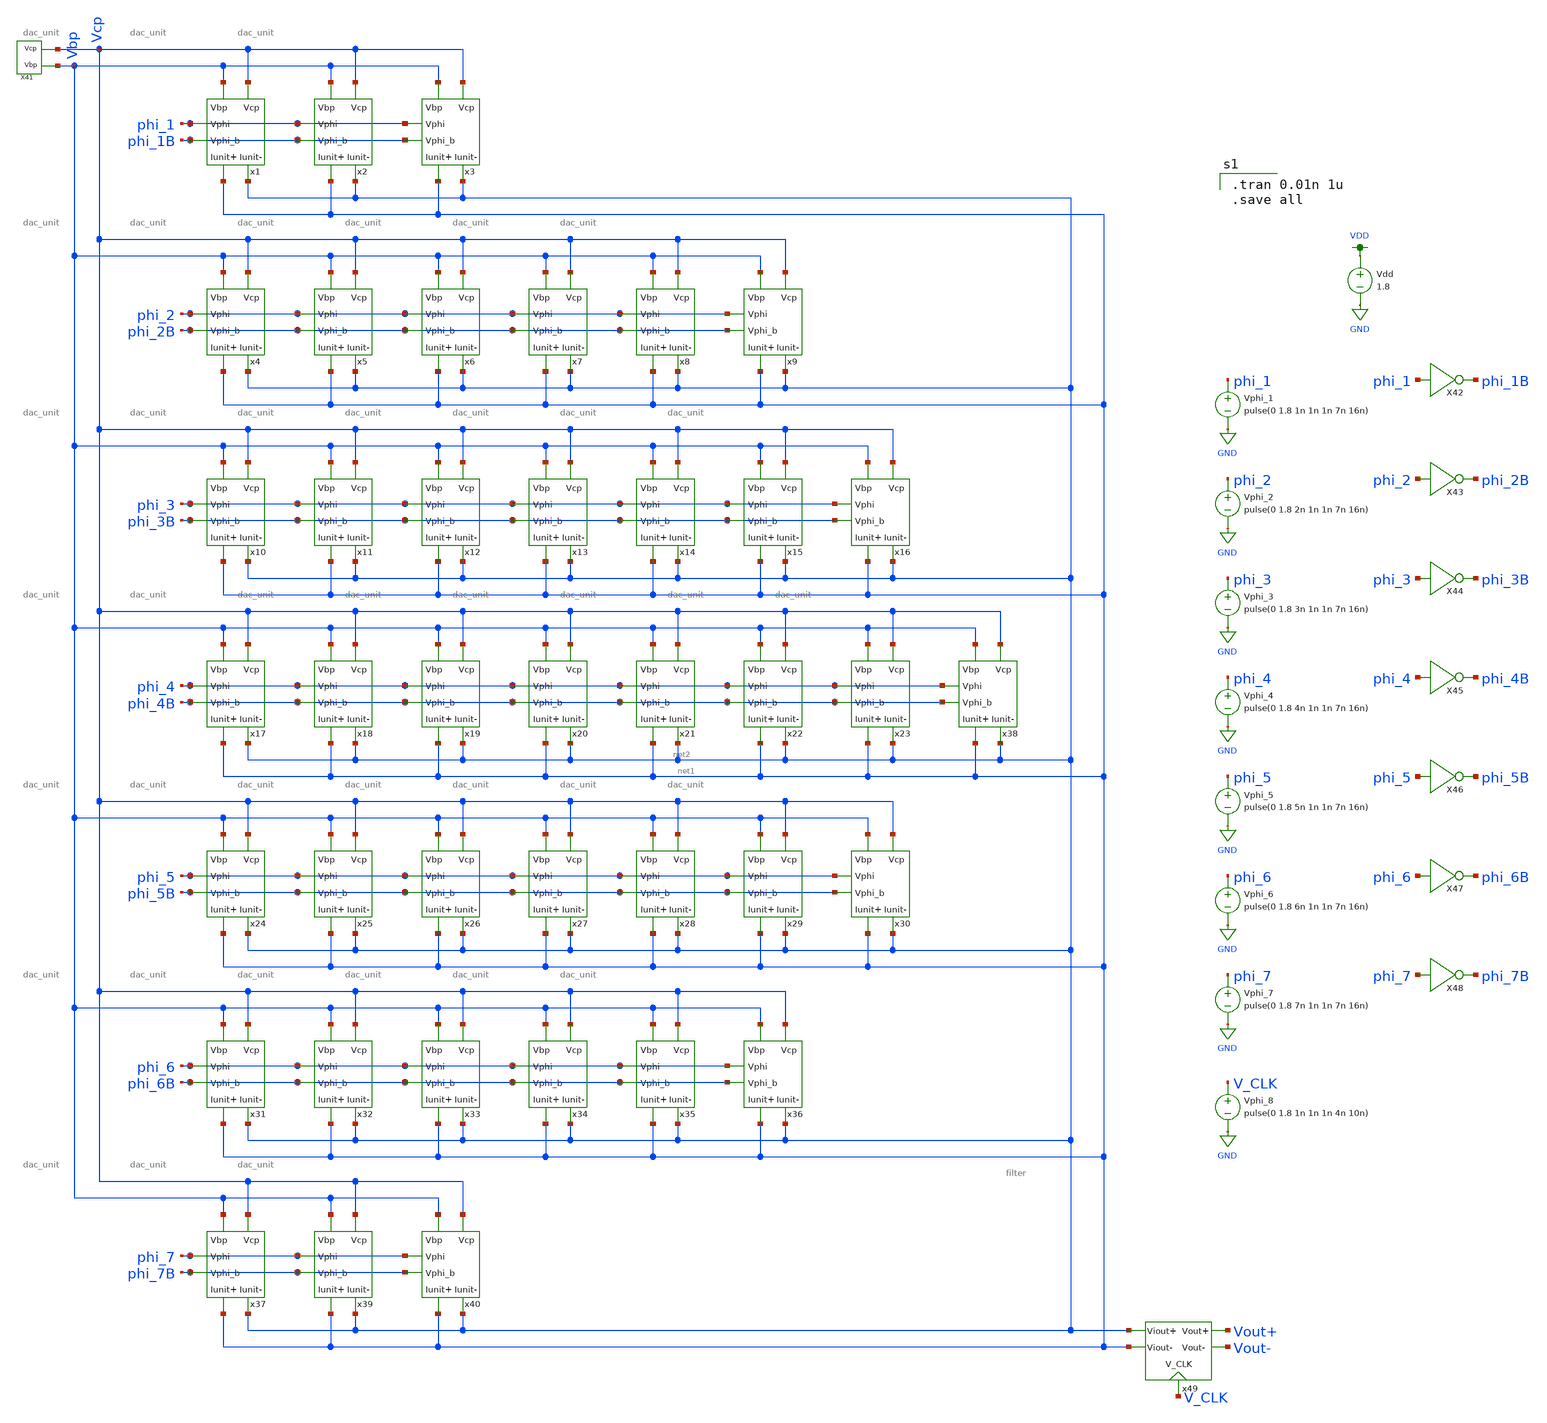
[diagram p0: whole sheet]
** sch_path: simulation/archived/dac_tran (copy).sch
**.subckt dac_tran (copy)
x1 Vbp Vcp net1 net2 phi_1 phi_1B dac_unit
x2 Vbp Vcp net1 net2 phi_1 phi_1B dac_unit
x3 Vbp Vcp net1 net2 phi_1 phi_1B dac_unit
x4 Vbp Vcp net1 net2 phi_2 phi_2B dac_unit
x5 Vbp Vcp net1 net2 phi_2 phi_2B dac_unit
x6 Vbp Vcp net1 net2 phi_2 phi_2B dac_unit
x7 Vbp Vcp net1 net2 phi_2 phi_2B dac_unit
x8 Vbp Vcp net1 net2 phi_2 phi_2B dac_unit
x9 Vbp Vcp net1 net2 phi_2 phi_2B dac_unit
x10 Vbp Vcp net1 net2 phi_3 phi_3B dac_unit
x11 Vbp Vcp net1 net2 phi_3 phi_3B dac_unit
x12 Vbp Vcp net1 net2 phi_3 phi_3B dac_unit
x13 Vbp Vcp net1 net2 phi_3 phi_3B dac_unit
x14 Vbp Vcp net1 net2 phi_3 phi_3B dac_unit
x15 Vbp Vcp net1 net2 phi_3 phi_3B dac_unit
x16 Vbp Vcp net1 net2 phi_3 phi_3B dac_unit
x17 Vbp Vcp net1 net2 phi_4 phi_4B dac_unit
x18 Vbp Vcp net1 net2 phi_4 phi_4B dac_unit
x19 Vbp Vcp net1 net2 phi_4 phi_4B dac_unit
x20 Vbp Vcp net1 net2 phi_4 phi_4B dac_unit
x21 Vbp Vcp net1 net2 phi_4 phi_4B dac_unit
x22 Vbp Vcp net1 net2 phi_4 phi_4B dac_unit
x23 Vbp Vcp net1 net2 phi_4 phi_4B dac_unit
x24 Vbp Vcp net1 net2 phi_5 phi_5B dac_unit
x25 Vbp Vcp net1 net2 phi_5 phi_5B dac_unit
x26 Vbp Vcp net1 net2 phi_5 phi_5B dac_unit
x27 Vbp Vcp net1 net2 phi_5 phi_5B dac_unit
x28 Vbp Vcp net1 net2 phi_5 phi_5B dac_unit
x29 Vbp Vcp net1 net2 phi_5 phi_5B dac_unit
x30 Vbp Vcp net1 net2 phi_5 phi_5B dac_unit
x31 Vbp Vcp net1 net2 phi_6 phi_6B dac_unit
x32 Vbp Vcp net1 net2 phi_6 phi_6B dac_unit
x33 Vbp Vcp net1 net2 phi_6 phi_6B dac_unit
x34 Vbp Vcp net1 net2 phi_6 phi_6B dac_unit
x35 Vbp Vcp net1 net2 phi_6 phi_6B dac_unit
x36 Vbp Vcp net1 net2 phi_6 phi_6B dac_unit
x38 Vbp Vcp net1 net2 phi_4 phi_4B dac_unit
x37 Vbp Vcp net1 net2 phi_7 phi_7B dac_unit
x39 Vbp Vcp net1 net2 phi_7 phi_7B dac_unit
x40 Vbp Vcp net1 net2 phi_7 phi_7B dac_unit
X41 Vcp Vbp v_gen_lds
Vdd VDD GND 1.8
Vphi_1 phi_1 GND pulse(0 1.8 1n 1n 1n 7n 16n)
Vphi_2 phi_2 GND pulse(0 1.8 2n 1n 1n 7n 16n)
Vphi_3 phi_3 GND pulse(0 1.8 3n 1n 1n 7n 16n)
Vphi_4 phi_4 GND pulse(0 1.8 4n 1n 1n 7n 16n)
Vphi_5 phi_5 GND pulse(0 1.8 5n 1n 1n 7n 16n)
Vphi_6 phi_6 GND pulse(0 1.8 6n 1n 1n 7n 16n)
Vphi_7 phi_7 GND pulse(0 1.8 7n 1n 1n 7n 16n)
X42 phi_1 phi_1B inverter
X43 phi_2 phi_2B inverter
X44 phi_3 phi_3B inverter
X45 phi_4 phi_4B inverter
X46 phi_5 phi_5B inverter
X47 phi_6 phi_6B inverter
X48 phi_7 phi_7B inverter
x49 net2 net1 Vout+ Vout- V_CLK filter
Vphi_8 V_CLK GND pulse(0 1.8 1n 1n 1n 4n 10n)
**** begin user architecture code

.tran 0.01n 1u
.save all


.option wnflag=1
.param MC_SWITCH=0.0
.lib ~/skywater/skywater-pdk/libraries/sky130_fd_pr_ngspice/latest/models/sky130.lib.spice tt

**** end user architecture code
**.ends

* expanding   symbol:  ./dac/dac_unit.sym # of pins=6
** sym_path: simulation/dac/dac_unit.sym
** sch_path: simulation/dac/dac_unit.sch
.subckt dac_unit Vbp Vcp Iunit+ Iunit- Vphi Vphi_b
*.ipin Vphi
*.ipin Vbp
*.ipin Vcp
*.opin Iunit-
*.opin Iunit+
*.ipin Vphi_b
XM1 net1 Vbp VDD VDD sky130_fd_pr__pfet_01v8 L=0.5 W=12 nf=1 ad='int((nf+1)/2) * W/nf * 0.29' as='int((nf+2)/2) * W/nf * 0.29'
+ pd='2*int((nf+1)/2) * (W/nf + 0.29)' ps='2*int((nf+2)/2) * (W/nf + 0.29)' nrd='0.29 / W' nrs='0.29 / W'
+ sa=0 sb=0 sd=0 mult=1 m=1
XM2 net2 Vcp net1 VDD sky130_fd_pr__pfet_01v8 L=0.5 W=12 nf=1 ad='int((nf+1)/2) * W/nf * 0.29' as='int((nf+2)/2) * W/nf * 0.29'
+ pd='2*int((nf+1)/2) * (W/nf + 0.29)' ps='2*int((nf+2)/2) * (W/nf + 0.29)' nrd='0.29 / W' nrs='0.29 / W'
+ sa=0 sb=0 sd=0 mult=1 m=1
XM3 Iunit- Vphi net2 VDD sky130_fd_pr__pfet_01v8 L=0.5 W=12 nf=1 ad='int((nf+1)/2) * W/nf * 0.29' as='int((nf+2)/2) * W/nf * 0.29'
+ pd='2*int((nf+1)/2) * (W/nf + 0.29)' ps='2*int((nf+2)/2) * (W/nf + 0.29)' nrd='0.29 / W' nrs='0.29 / W'
+ sa=0 sb=0 sd=0 mult=1 m=1
XM4 Iunit+ Vphi_b net2 VDD sky130_fd_pr__pfet_01v8 L=0.5 W=12 nf=1 ad='int((nf+1)/2) * W/nf * 0.29' as='int((nf+2)/2) * W/nf * 0.29'
+ pd='2*int((nf+1)/2) * (W/nf + 0.29)' ps='2*int((nf+2)/2) * (W/nf + 0.29)' nrd='0.29 / W' nrs='0.29 / W'
+ sa=0 sb=0 sd=0 mult=1 m=1
.ends


* expanding   symbol:  ./dac/v_gen_lds.sym # of pins=2
** sym_path: simulation/dac/v_gen_lds.sym
** sch_path: simulation/dac/v_gen_lds.sch
.subckt v_gen_lds Vcp Vbp
*.opin Vcp
*.opin Vbp
XM25 net1 Vcp Vcp VDD sky130_fd_pr__pfet_01v8 L=0.5 W=12 nf=1 ad='int((nf+1)/2) * W/nf * 0.29' as='int((nf+2)/2) * W/nf * 0.29'
+ pd='2*int((nf+1)/2) * (W/nf + 0.29)' ps='2*int((nf+2)/2) * (W/nf + 0.29)' nrd='0.29 / W' nrs='0.29 / W'
+ sa=0 sb=0 sd=0 mult=1 m=1
XM26 Vcp net3 GND GND sky130_fd_pr__nfet_01v8 L=0.5 W=12 nf=1 ad='int((nf+1)/2) * W/nf * 0.29' as='int((nf+2)/2) * W/nf * 0.29'
+ pd='2*int((nf+1)/2) * (W/nf + 0.29)' ps='2*int((nf+2)/2) * (W/nf + 0.29)' nrd='0.29 / W' nrs='0.29 / W'
+ sa=0 sb=0 sd=0 mult=1 m=1
XM27 net2 net2 net1 VDD sky130_fd_pr__pfet_01v8 L=0.5 W=12 nf=1 ad='int((nf+1)/2) * W/nf * 0.29' as='int((nf+2)/2) * W/nf * 0.29'
+ pd='2*int((nf+1)/2) * (W/nf + 0.29)' ps='2*int((nf+2)/2) * (W/nf + 0.29)' nrd='0.29 / W' nrs='0.29 / W'
+ sa=0 sb=0 sd=0 mult=1 m=1
XM28 GND net3 net4 GND sky130_fd_pr__nfet_01v8 L=0.5 W=12 nf=1 ad='int((nf+1)/2) * W/nf * 0.29' as='int((nf+2)/2) * W/nf * 0.29'
+ pd='2*int((nf+1)/2) * (W/nf + 0.29)' ps='2*int((nf+2)/2) * (W/nf + 0.29)' nrd='0.29 / W' nrs='0.29 / W'
+ sa=0 sb=0 sd=0 mult=1 m=1
XM41 net1 net2 net2 VDD sky130_fd_pr__pfet_01v8 L=0.5 W=12 nf=1 ad='int((nf+1)/2) * W/nf * 0.29' as='int((nf+2)/2) * W/nf * 0.29'
+ pd='2*int((nf+1)/2) * (W/nf + 0.29)' ps='2*int((nf+2)/2) * (W/nf + 0.29)' nrd='0.29 / W' nrs='0.29 / W'
+ sa=0 sb=0 sd=0 mult=1 m=1
XM42 net4 net3 net5 GND sky130_fd_pr__nfet_01v8 L=0.5 W=12 nf=1 ad='int((nf+1)/2) * W/nf * 0.29' as='int((nf+2)/2) * W/nf * 0.29'
+ pd='2*int((nf+1)/2) * (W/nf + 0.29)' ps='2*int((nf+2)/2) * (W/nf + 0.29)' nrd='0.29 / W' nrs='0.29 / W'
+ sa=0 sb=0 sd=0 mult=1 m=1
XM43 net2 net2 net1 VDD sky130_fd_pr__pfet_01v8 L=0.5 W=12 nf=1 ad='int((nf+1)/2) * W/nf * 0.29' as='int((nf+2)/2) * W/nf * 0.29'
+ pd='2*int((nf+1)/2) * (W/nf + 0.29)' ps='2*int((nf+2)/2) * (W/nf + 0.29)' nrd='0.29 / W' nrs='0.29 / W'
+ sa=0 sb=0 sd=0 mult=1 m=1
XM44 net5 net3 net6 GND sky130_fd_pr__nfet_01v8 L=0.5 W=12 nf=1 ad='int((nf+1)/2) * W/nf * 0.29' as='int((nf+2)/2) * W/nf * 0.29'
+ pd='2*int((nf+1)/2) * (W/nf + 0.29)' ps='2*int((nf+2)/2) * (W/nf + 0.29)' nrd='0.29 / W' nrs='0.29 / W'
+ sa=0 sb=0 sd=0 mult=1 m=1
XM45 net1 net2 net2 VDD sky130_fd_pr__pfet_01v8 L=0.5 W=12 nf=1 ad='int((nf+1)/2) * W/nf * 0.29' as='int((nf+2)/2) * W/nf * 0.29'
+ pd='2*int((nf+1)/2) * (W/nf + 0.29)' ps='2*int((nf+2)/2) * (W/nf + 0.29)' nrd='0.29 / W' nrs='0.29 / W'
+ sa=0 sb=0 sd=0 mult=1 m=1
XM46 net6 net3 net7 GND sky130_fd_pr__nfet_01v8 L=0.5 W=12 nf=1 ad='int((nf+1)/2) * W/nf * 0.29' as='int((nf+2)/2) * W/nf * 0.29'
+ pd='2*int((nf+1)/2) * (W/nf + 0.29)' ps='2*int((nf+2)/2) * (W/nf + 0.29)' nrd='0.29 / W' nrs='0.29 / W'
+ sa=0 sb=0 sd=0 mult=1 m=1
XM47 VDD net2 net1 VDD sky130_fd_pr__pfet_01v8 L=0.5 W=12 nf=1 ad='int((nf+1)/2) * W/nf * 0.29' as='int((nf+2)/2) * W/nf * 0.29'
+ pd='2*int((nf+1)/2) * (W/nf + 0.29)' ps='2*int((nf+2)/2) * (W/nf + 0.29)' nrd='0.29 / W' nrs='0.29 / W'
+ sa=0 sb=0 sd=0 mult=1 m=1
XM48 net7 net3 net2 GND sky130_fd_pr__nfet_01v8 L=0.5 W=12 nf=1 ad='int((nf+1)/2) * W/nf * 0.29' as='int((nf+2)/2) * W/nf * 0.29'
+ pd='2*int((nf+1)/2) * (W/nf + 0.29)' ps='2*int((nf+2)/2) * (W/nf + 0.29)' nrd='0.29 / W' nrs='0.29 / W'
+ sa=0 sb=0 sd=0 mult=1 m=1
XM54 VDD Vbp Vbp VDD sky130_fd_pr__pfet_01v8 L=0.5 W=12 nf=1 ad='int((nf+1)/2) * W/nf * 0.29' as='int((nf+2)/2) * W/nf * 0.29'
+ pd='2*int((nf+1)/2) * (W/nf + 0.29)' ps='2*int((nf+2)/2) * (W/nf + 0.29)' nrd='0.29 / W' nrs='0.29 / W'
+ sa=0 sb=0 sd=0 mult=1 m=1
XM1 Vbp net3 GND GND sky130_fd_pr__nfet_01v8 L=0.5 W=12 nf=1 ad='int((nf+1)/2) * W/nf * 0.29' as='int((nf+2)/2) * W/nf * 0.29'
+ pd='2*int((nf+1)/2) * (W/nf + 0.29)' ps='2*int((nf+2)/2) * (W/nf + 0.29)' nrd='0.29 / W' nrs='0.29 / W'
+ sa=0 sb=0 sd=0 mult=1 m=1
XM2 net3 net3 GND GND sky130_fd_pr__nfet_01v8 L=0.5 W=12 nf=1 ad='int((nf+1)/2) * W/nf * 0.29' as='int((nf+2)/2) * W/nf * 0.29'
+ pd='2*int((nf+1)/2) * (W/nf + 0.29)' ps='2*int((nf+2)/2) * (W/nf + 0.29)' nrd='0.29 / W' nrs='0.29 / W'
+ sa=0 sb=0 sd=0 mult=1 m=1
XM3 Vcp VDD VDD VDD sky130_fd_pr__pfet_01v8 L=0.5 W=12 nf=1 ad='int((nf+1)/2) * W/nf * 0.29' as='int((nf+2)/2) * W/nf * 0.29'
+ pd='2*int((nf+1)/2) * (W/nf + 0.29)' ps='2*int((nf+2)/2) * (W/nf + 0.29)' nrd='0.29 / W' nrs='0.29 / W'
+ sa=0 sb=0 sd=0 mult=1 m=1
XM16 net8 net13 net13 VDD sky130_fd_pr__pfet_01v8 L=0.5 W=12 nf=1 ad='int((nf+1)/2) * W/nf * 0.29' as='int((nf+2)/2) * W/nf * 0.29'
+ pd='2*int((nf+1)/2) * (W/nf + 0.29)' ps='2*int((nf+2)/2) * (W/nf + 0.29)' nrd='0.29 / W' nrs='0.29 / W'
+ sa=0 sb=0 sd=0 mult=1 m=1
XM17 net13 net3 GND GND sky130_fd_pr__nfet_01v8 L=0.5 W=12 nf=1 ad='int((nf+1)/2) * W/nf * 0.29' as='int((nf+2)/2) * W/nf * 0.29'
+ pd='2*int((nf+1)/2) * (W/nf + 0.29)' ps='2*int((nf+2)/2) * (W/nf + 0.29)' nrd='0.29 / W' nrs='0.29 / W'
+ sa=0 sb=0 sd=0 mult=1 m=1
XM18 net2 net2 net8 VDD sky130_fd_pr__pfet_01v8 L=0.5 W=12 nf=1 ad='int((nf+1)/2) * W/nf * 0.29' as='int((nf+2)/2) * W/nf * 0.29'
+ pd='2*int((nf+1)/2) * (W/nf + 0.29)' ps='2*int((nf+2)/2) * (W/nf + 0.29)' nrd='0.29 / W' nrs='0.29 / W'
+ sa=0 sb=0 sd=0 mult=1 m=1
XM19 GND net3 net9 GND sky130_fd_pr__nfet_01v8 L=0.5 W=12 nf=1 ad='int((nf+1)/2) * W/nf * 0.29' as='int((nf+2)/2) * W/nf * 0.29'
+ pd='2*int((nf+1)/2) * (W/nf + 0.29)' ps='2*int((nf+2)/2) * (W/nf + 0.29)' nrd='0.29 / W' nrs='0.29 / W'
+ sa=0 sb=0 sd=0 mult=1 m=1
XM20 net8 net2 net2 VDD sky130_fd_pr__pfet_01v8 L=0.5 W=12 nf=1 ad='int((nf+1)/2) * W/nf * 0.29' as='int((nf+2)/2) * W/nf * 0.29'
+ pd='2*int((nf+1)/2) * (W/nf + 0.29)' ps='2*int((nf+2)/2) * (W/nf + 0.29)' nrd='0.29 / W' nrs='0.29 / W'
+ sa=0 sb=0 sd=0 mult=1 m=1
XM21 net9 net3 net10 GND sky130_fd_pr__nfet_01v8 L=0.5 W=12 nf=1 ad='int((nf+1)/2) * W/nf * 0.29' as='int((nf+2)/2) * W/nf * 0.29'
+ pd='2*int((nf+1)/2) * (W/nf + 0.29)' ps='2*int((nf+2)/2) * (W/nf + 0.29)' nrd='0.29 / W' nrs='0.29 / W'
+ sa=0 sb=0 sd=0 mult=1 m=1
XM22 net2 net2 net8 VDD sky130_fd_pr__pfet_01v8 L=0.5 W=12 nf=1 ad='int((nf+1)/2) * W/nf * 0.29' as='int((nf+2)/2) * W/nf * 0.29'
+ pd='2*int((nf+1)/2) * (W/nf + 0.29)' ps='2*int((nf+2)/2) * (W/nf + 0.29)' nrd='0.29 / W' nrs='0.29 / W'
+ sa=0 sb=0 sd=0 mult=1 m=1
XM23 net10 net3 net11 GND sky130_fd_pr__nfet_01v8 L=0.5 W=12 nf=1 ad='int((nf+1)/2) * W/nf * 0.29' as='int((nf+2)/2) * W/nf * 0.29'
+ pd='2*int((nf+1)/2) * (W/nf + 0.29)' ps='2*int((nf+2)/2) * (W/nf + 0.29)' nrd='0.29 / W' nrs='0.29 / W'
+ sa=0 sb=0 sd=0 mult=1 m=1
XM24 net8 net2 net2 VDD sky130_fd_pr__pfet_01v8 L=0.5 W=12 nf=1 ad='int((nf+1)/2) * W/nf * 0.29' as='int((nf+2)/2) * W/nf * 0.29'
+ pd='2*int((nf+1)/2) * (W/nf + 0.29)' ps='2*int((nf+2)/2) * (W/nf + 0.29)' nrd='0.29 / W' nrs='0.29 / W'
+ sa=0 sb=0 sd=0 mult=1 m=1
XM49 net11 net3 net12 GND sky130_fd_pr__nfet_01v8 L=0.5 W=12 nf=1 ad='int((nf+1)/2) * W/nf * 0.29' as='int((nf+2)/2) * W/nf * 0.29'
+ pd='2*int((nf+1)/2) * (W/nf + 0.29)' ps='2*int((nf+2)/2) * (W/nf + 0.29)' nrd='0.29 / W' nrs='0.29 / W'
+ sa=0 sb=0 sd=0 mult=1 m=1
XM50 VDD net2 net8 VDD sky130_fd_pr__pfet_01v8 L=0.5 W=12 nf=1 ad='int((nf+1)/2) * W/nf * 0.29' as='int((nf+2)/2) * W/nf * 0.29'
+ pd='2*int((nf+1)/2) * (W/nf + 0.29)' ps='2*int((nf+2)/2) * (W/nf + 0.29)' nrd='0.29 / W' nrs='0.29 / W'
+ sa=0 sb=0 sd=0 mult=1 m=1
XM51 net12 net3 net2 GND sky130_fd_pr__nfet_01v8 L=0.5 W=12 nf=1 ad='int((nf+1)/2) * W/nf * 0.29' as='int((nf+2)/2) * W/nf * 0.29'
+ pd='2*int((nf+1)/2) * (W/nf + 0.29)' ps='2*int((nf+2)/2) * (W/nf + 0.29)' nrd='0.29 / W' nrs='0.29 / W'
+ sa=0 sb=0 sd=0 mult=1 m=1
XM52 VDD Vbp Vbp VDD sky130_fd_pr__pfet_01v8 L=0.5 W=12 nf=1 ad='int((nf+1)/2) * W/nf * 0.29' as='int((nf+2)/2) * W/nf * 0.29'
+ pd='2*int((nf+1)/2) * (W/nf + 0.29)' ps='2*int((nf+2)/2) * (W/nf + 0.29)' nrd='0.29 / W' nrs='0.29 / W'
+ sa=0 sb=0 sd=0 mult=1 m=1
XM53 GND net3 Vbp GND sky130_fd_pr__nfet_01v8 L=0.5 W=12 nf=1 ad='int((nf+1)/2) * W/nf * 0.29' as='int((nf+2)/2) * W/nf * 0.29'
+ pd='2*int((nf+1)/2) * (W/nf + 0.29)' ps='2*int((nf+2)/2) * (W/nf + 0.29)' nrd='0.29 / W' nrs='0.29 / W'
+ sa=0 sb=0 sd=0 mult=1 m=1
XM55 net3 net3 GND GND sky130_fd_pr__nfet_01v8 L=0.5 W=12 nf=1 ad='int((nf+1)/2) * W/nf * 0.29' as='int((nf+2)/2) * W/nf * 0.29'
+ pd='2*int((nf+1)/2) * (W/nf + 0.29)' ps='2*int((nf+2)/2) * (W/nf + 0.29)' nrd='0.29 / W' nrs='0.29 / W'
+ sa=0 sb=0 sd=0 mult=1 m=1
XM56 net13 VDD VDD VDD sky130_fd_pr__pfet_01v8 L=0.5 W=12 nf=1 ad='int((nf+1)/2) * W/nf * 0.29' as='int((nf+2)/2) * W/nf * 0.29'
+ pd='2*int((nf+1)/2) * (W/nf + 0.29)' ps='2*int((nf+2)/2) * (W/nf + 0.29)' nrd='0.29 / W' nrs='0.29 / W'
+ sa=0 sb=0 sd=0 mult=1 m=1
Ib GND net3 2u
.ends


* expanding   symbol:  ./dac/inverter.sym # of pins=2
** sym_path: simulation/dac/inverter.sym
** sch_path: simulation/dac/inverter.sch
.subckt inverter A Y
*.ipin A
*.opin Y
XM1 Y A VDD VDD sky130_fd_pr__pfet_01v8 L=0.15 W=1 nf=1 ad='int((nf+1)/2) * W/nf * 0.29' as='int((nf+2)/2) * W/nf * 0.29'
+ pd='2*int((nf+1)/2) * (W/nf + 0.29)' ps='2*int((nf+2)/2) * (W/nf + 0.29)' nrd='0.29 / W' nrs='0.29 / W'
+ sa=0 sb=0 sd=0 mult=1 m=1
XM2 Y A GND GND sky130_fd_pr__nfet_01v8 L=0.15 W=1 nf=1 ad='int((nf+1)/2) * W/nf * 0.29' as='int((nf+2)/2) * W/nf * 0.29'
+ pd='2*int((nf+1)/2) * (W/nf + 0.29)' ps='2*int((nf+2)/2) * (W/nf + 0.29)' nrd='0.29 / W' nrs='0.29 / W'
+ sa=0 sb=0 sd=0 mult=1 m=1
.ends


* expanding   symbol:  /home/madvlsi/VLSI_Sine_Gen/simulation/filter/filter.sym # of pins=5
** sym_path: simulation/filter/filter.sym
** sch_path: simulation/filter/filter.sch
.subckt filter Viout+ Viout- Vout+ Vout- V_CLK
*.ipin Viout+
*.ipin Viout-
*.opin Vout+
*.opin Vout-
*.ipin V_CLK
C1 Vout- Vout+ 5n m=1
C3 net3 GND 1n m=1
XM1 net3 net1 Vout+ GND sky130_fd_pr__nfet_01v8 L=0.15 W=1 nf=1 ad='int((nf+1)/2) * W/nf * 0.29' as='int((nf+2)/2) * W/nf * 0.29'
+ pd='2*int((nf+1)/2) * (W/nf + 0.29)' ps='2*int((nf+2)/2) * (W/nf + 0.29)' nrd='0.29 / W' nrs='0.29 / W'
+ sa=0 sb=0 sd=0 mult=1 m=1
XM2 Viout+ V_CLK net3 GND sky130_fd_pr__nfet_01v8 L=0.15 W=1 nf=1 ad='int((nf+1)/2) * W/nf * 0.29' as='int((nf+2)/2) * W/nf * 0.29'
+ pd='2*int((nf+1)/2) * (W/nf + 0.29)' ps='2*int((nf+2)/2) * (W/nf + 0.29)' nrd='0.29 / W' nrs='0.29 / W'
+ sa=0 sb=0 sd=0 mult=1 m=1
C4 Viout+ GND 1n m=1
X1 V_CLK net1 inverter
C5 net2 GND 1n m=1
XM3 net2 net1 Vout- GND sky130_fd_pr__nfet_01v8 L=0.15 W=1 nf=1 ad='int((nf+1)/2) * W/nf * 0.29' as='int((nf+2)/2) * W/nf * 0.29'
+ pd='2*int((nf+1)/2) * (W/nf + 0.29)' ps='2*int((nf+2)/2) * (W/nf + 0.29)' nrd='0.29 / W' nrs='0.29 / W'
+ sa=0 sb=0 sd=0 mult=1 m=1
XM4 Viout- V_CLK net2 GND sky130_fd_pr__nfet_01v8 L=0.15 W=1 nf=1 ad='int((nf+1)/2) * W/nf * 0.29' as='int((nf+2)/2) * W/nf * 0.29'
+ pd='2*int((nf+1)/2) * (W/nf + 0.29)' ps='2*int((nf+2)/2) * (W/nf + 0.29)' nrd='0.29 / W' nrs='0.29 / W'
+ sa=0 sb=0 sd=0 mult=1 m=1
C6 Viout- GND 1n m=1
.ends

.GLOBAL VDD
.GLOBAL GND
.end
